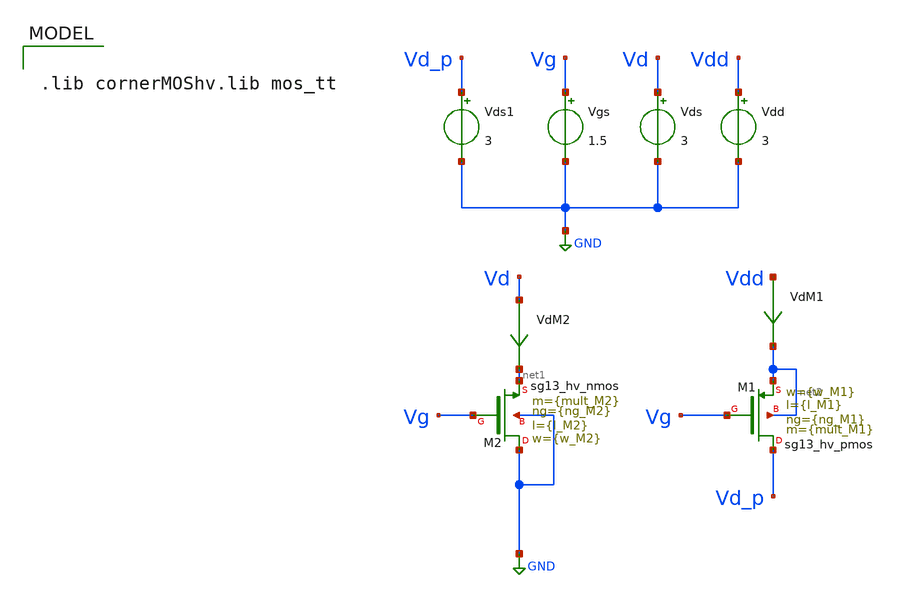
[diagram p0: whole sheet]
** sch_path: xschem/TB_hvMOS_POWER_Sizing.sch
**.subckt TB_hvMOS_POWER_Sizing
Vgs Vg GND 1.5
Vds Vd GND 3
Vdd Vdd GND 3
XM2 GND Vg net1 GND sg13_hv_nmos w={w_M2} l={l_M2} ng={ng_M2} m={mult_M2} mm_ok=1
VdM1 Vdd net2 0
.save i(vdm1)
XM1 Vd_p Vg net2 net2 sg13_hv_pmos w={w_M1} l={l_M1} ng={ng_M1} m={mult_M1} mm_ok=1
VdM2 Vd net1 0
.save i(vdm2)
Vds1 Vd_p GND 3
**** begin user architecture code

.lib cornerMOShv.lib mos_tt



.save all
* + @M.XM1.m1[id]  @n.xm1.nsg13_hv_nmos[vth]  @n.xm2.nsg13_hv_pmos[vth]

.control
reset
alter Vgs 3
dc Vds 0 1 0.01
*dc Vds 0 0.5 0.01 temp 0 27 1

plot i(VdM2)

print @n.xm1.nsg13_hv_nmos[vth]
*print @n.xm2.nsg13_hv_nmos[vth]
.endc

.control
reset
alter Vgs 0
dc Vds1 2 3 0.01
*dc Vds 0 0.5 0.01 temp 0 27 1

plot i(VdM1)

print @n.xm2.nsg13_hv_pmos[vth]
.endc

.control
reset
alter Vgs 3
dc Vds1 0 3 0.01
plot i(VdM1)

print @n.xm2.nsg13_hv_pmos[vth]
.end




.param temp=27
.param mult_M1 = 2400
.param w_M1 =10u
*.param l_M1 = 0.2u ** Posee mayor capacidad de corriente, pero en sub-umbral conduce mucha
*+ corriente
.param l_M1 = 0.22u
.param ng_M1 = 1

.param mult_M2 = 1200
.param w_M2 =10u
*.param l_M2 =0.25u
.param l_M2 =0.25u
.param ng_M2 =1





**** end user architecture code
**.ends
.GLOBAL GND
.end
